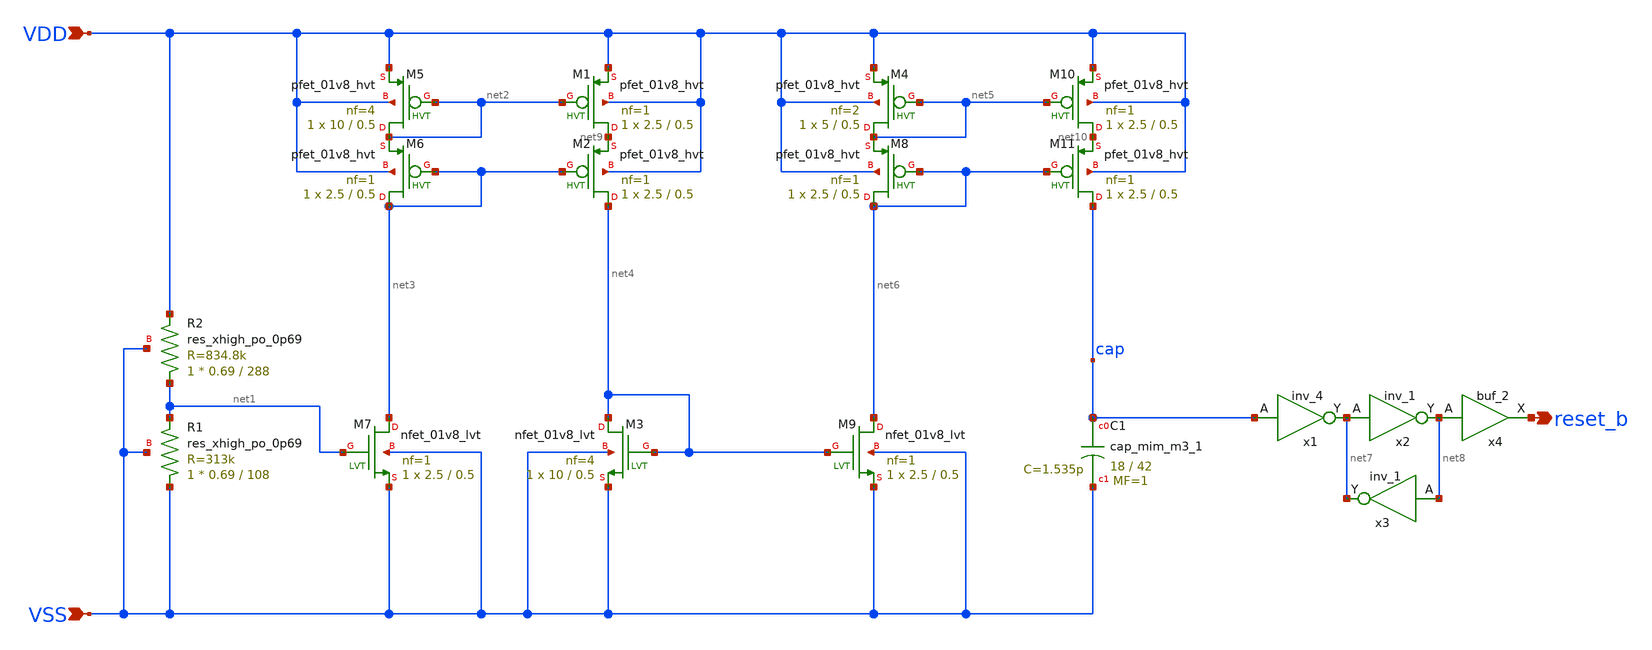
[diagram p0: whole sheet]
** sch_path: xschem/por.sch
**.subckt por VDD VSS reset_b
*.ipin VDD
*.ipin VSS
*.opin reset_b
XC1 cap VSS sky130_fd_pr__cap_mim_m3_1 W=18 L=42 MF=1 m=1
x1 cap VSS VSS VDD VDD net7 sky130_fd_sc_hd__inv_4
XR1 VSS net1 VSS sky130_fd_pr__res_xhigh_po_0p69 L=108 mult=1 m=1
XM5 net2 net2 VDD VDD sky130_fd_pr__pfet_01v8_hvt L=0.5 W=10 nf=4 ad='int((nf+1)/2) * W/nf * 0.29' as='int((nf+2)/2) * W/nf * 0.29'
+ pd='2*int((nf+1)/2) * (W/nf + 0.29)' ps='2*int((nf+2)/2) * (W/nf + 0.29)' nrd='0.29 / W' nrs='0.29 / W'
+ sa=0 sb=0 sd=0 mult=1 m=1
XM6 net3 net3 net2 VDD sky130_fd_pr__pfet_01v8_hvt L=0.5 W=2.5 nf=1 ad='int((nf+1)/2) * W/nf * 0.29'
+ as='int((nf+2)/2) * W/nf * 0.29' pd='2*int((nf+1)/2) * (W/nf + 0.29)' ps='2*int((nf+2)/2) * (W/nf + 0.29)'
+ nrd='0.29 / W' nrs='0.29 / W' sa=0 sb=0 sd=0 mult=1 m=1
XM7 net3 net1 VSS VSS sky130_fd_pr__nfet_01v8_lvt L=0.5 W=2.5 nf=1 ad='int((nf+1)/2) * W/nf * 0.29' as='int((nf+2)/2) * W/nf * 0.29'
+ pd='2*int((nf+1)/2) * (W/nf + 0.29)' ps='2*int((nf+2)/2) * (W/nf + 0.29)' nrd='0.29 / W' nrs='0.29 / W'
+ sa=0 sb=0 sd=0 mult=1 m=1
XR2 net1 VDD VSS sky130_fd_pr__res_xhigh_po_0p69 L=288 mult=1 m=1
XM1 net9 net2 VDD VDD sky130_fd_pr__pfet_01v8_hvt L=0.5 W=2.5 nf=1 ad='int((nf+1)/2) * W/nf * 0.29' as='int((nf+2)/2) * W/nf * 0.29'
+ pd='2*int((nf+1)/2) * (W/nf + 0.29)' ps='2*int((nf+2)/2) * (W/nf + 0.29)' nrd='0.29 / W' nrs='0.29 / W'
+ sa=0 sb=0 sd=0 mult=1 m=1
XM2 net4 net3 net9 VDD sky130_fd_pr__pfet_01v8_hvt L=0.5 W=2.5 nf=1 ad='int((nf+1)/2) * W/nf * 0.29'
+ as='int((nf+2)/2) * W/nf * 0.29' pd='2*int((nf+1)/2) * (W/nf + 0.29)' ps='2*int((nf+2)/2) * (W/nf + 0.29)'
+ nrd='0.29 / W' nrs='0.29 / W' sa=0 sb=0 sd=0 mult=1 m=1
XM3 net4 net4 VSS VSS sky130_fd_pr__nfet_01v8_lvt L=0.5 W=10 nf=4 ad='int((nf+1)/2) * W/nf * 0.29' as='int((nf+2)/2) * W/nf * 0.29'
+ pd='2*int((nf+1)/2) * (W/nf + 0.29)' ps='2*int((nf+2)/2) * (W/nf + 0.29)' nrd='0.29 / W' nrs='0.29 / W'
+ sa=0 sb=0 sd=0 mult=1 m=1
XM4 net5 net5 VDD VDD sky130_fd_pr__pfet_01v8_hvt L=0.5 W=5 nf=2 ad='int((nf+1)/2) * W/nf * 0.29' as='int((nf+2)/2) * W/nf * 0.29'
+ pd='2*int((nf+1)/2) * (W/nf + 0.29)' ps='2*int((nf+2)/2) * (W/nf + 0.29)' nrd='0.29 / W' nrs='0.29 / W'
+ sa=0 sb=0 sd=0 mult=1 m=1
XM8 net6 net6 net5 VDD sky130_fd_pr__pfet_01v8_hvt L=0.5 W=2.5 nf=1 ad='int((nf+1)/2) * W/nf * 0.29'
+ as='int((nf+2)/2) * W/nf * 0.29' pd='2*int((nf+1)/2) * (W/nf + 0.29)' ps='2*int((nf+2)/2) * (W/nf + 0.29)'
+ nrd='0.29 / W' nrs='0.29 / W' sa=0 sb=0 sd=0 mult=1 m=1
XM9 net6 net4 VSS VSS sky130_fd_pr__nfet_01v8_lvt L=0.5 W=2.5 nf=1 ad='int((nf+1)/2) * W/nf * 0.29' as='int((nf+2)/2) * W/nf * 0.29'
+ pd='2*int((nf+1)/2) * (W/nf + 0.29)' ps='2*int((nf+2)/2) * (W/nf + 0.29)' nrd='0.29 / W' nrs='0.29 / W'
+ sa=0 sb=0 sd=0 mult=1 m=1
XM10 net10 net5 VDD VDD sky130_fd_pr__pfet_01v8_hvt L=0.5 W=2.5 nf=1 ad='int((nf+1)/2) * W/nf * 0.29'
+ as='int((nf+2)/2) * W/nf * 0.29' pd='2*int((nf+1)/2) * (W/nf + 0.29)' ps='2*int((nf+2)/2) * (W/nf + 0.29)'
+ nrd='0.29 / W' nrs='0.29 / W' sa=0 sb=0 sd=0 mult=1 m=1
XM11 cap net6 net10 VDD sky130_fd_pr__pfet_01v8_hvt L=0.5 W=2.5 nf=1 ad='int((nf+1)/2) * W/nf * 0.29'
+ as='int((nf+2)/2) * W/nf * 0.29' pd='2*int((nf+1)/2) * (W/nf + 0.29)' ps='2*int((nf+2)/2) * (W/nf + 0.29)'
+ nrd='0.29 / W' nrs='0.29 / W' sa=0 sb=0 sd=0 mult=1 m=1
x2 net7 VSS VSS VDD VDD net8 sky130_fd_sc_hd__inv_1
x3 net8 VSS VSS VDD VDD net7 sky130_fd_sc_hd__inv_1
x4 net8 VSS VSS VDD VDD reset_b sky130_fd_sc_hd__buf_2
**.ends
.end
